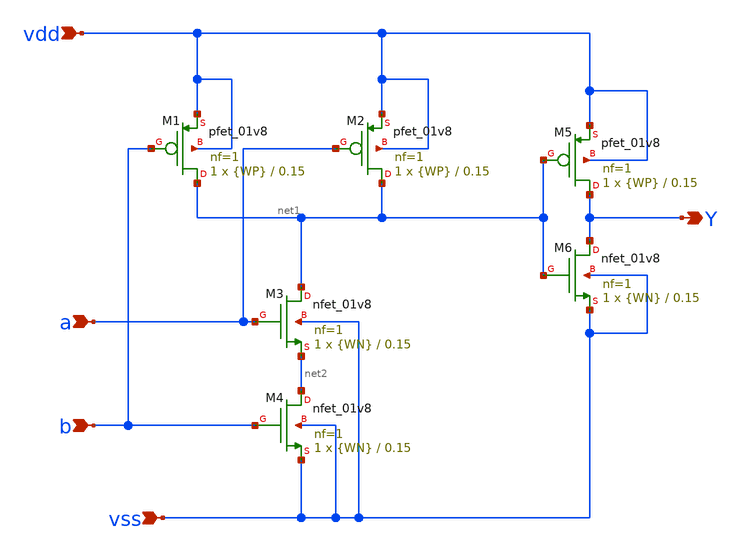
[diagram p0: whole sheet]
** sch_path: eamta2021/sch/and/and.sch
**.subckt and vdd vss a b Y
*.ipin vdd
*.ipin vss
*.ipin a
*.ipin b
*.opin Y
XM1 net1 b vdd vdd sky130_fd_pr__pfet_01v8 L=0.15 W={WP} nf=1 ad='int((nf+1)/2) * W/nf * 0.29' as='int((nf+2)/2) * W/nf * 0.29'
+ pd='2*int((nf+1)/2) * (W/nf + 0.29)' ps='2*int((nf+2)/2) * (W/nf + 0.29)' nrd='0.29 / W' nrs='0.29 / W'
+ sa=0 sb=0 sd=0 mult=1 m=1
XM2 net1 a vdd vdd sky130_fd_pr__pfet_01v8 L=0.15 W={WP} nf=1 ad='int((nf+1)/2) * W/nf * 0.29' as='int((nf+2)/2) * W/nf * 0.29'
+ pd='2*int((nf+1)/2) * (W/nf + 0.29)' ps='2*int((nf+2)/2) * (W/nf + 0.29)' nrd='0.29 / W' nrs='0.29 / W'
+ sa=0 sb=0 sd=0 mult=1 m=1
XM3 net1 a net2 vss sky130_fd_pr__nfet_01v8 L=0.15 W={WN} nf=1 ad='int((nf+1)/2) * W/nf * 0.29' as='int((nf+2)/2) * W/nf * 0.29'
+ pd='2*int((nf+1)/2) * (W/nf + 0.29)' ps='2*int((nf+2)/2) * (W/nf + 0.29)' nrd='0.29 / W' nrs='0.29 / W'
+ sa=0 sb=0 sd=0 mult=1 m=1
XM4 net2 b vss vss sky130_fd_pr__nfet_01v8 L=0.15 W={WN} nf=1 ad='int((nf+1)/2) * W/nf * 0.29' as='int((nf+2)/2) * W/nf * 0.29'
+ pd='2*int((nf+1)/2) * (W/nf + 0.29)' ps='2*int((nf+2)/2) * (W/nf + 0.29)' nrd='0.29 / W' nrs='0.29 / W'
+ sa=0 sb=0 sd=0 mult=1 m=1
XM5 Y net1 vdd vdd sky130_fd_pr__pfet_01v8 L=0.15 W={WP} nf=1 ad='int((nf+1)/2) * W/nf * 0.29' as='int((nf+2)/2) * W/nf * 0.29'
+ pd='2*int((nf+1)/2) * (W/nf + 0.29)' ps='2*int((nf+2)/2) * (W/nf + 0.29)' nrd='0.29 / W' nrs='0.29 / W'
+ sa=0 sb=0 sd=0 mult=1 m=1
XM6 Y net1 vss vss sky130_fd_pr__nfet_01v8 L=0.15 W={WN} nf=1 ad='int((nf+1)/2) * W/nf * 0.29' as='int((nf+2)/2) * W/nf * 0.29'
+ pd='2*int((nf+1)/2) * (W/nf + 0.29)' ps='2*int((nf+2)/2) * (W/nf + 0.29)' nrd='0.29 / W' nrs='0.29 / W'
+ sa=0 sb=0 sd=0 mult=1 m=1
**.ends
.end
